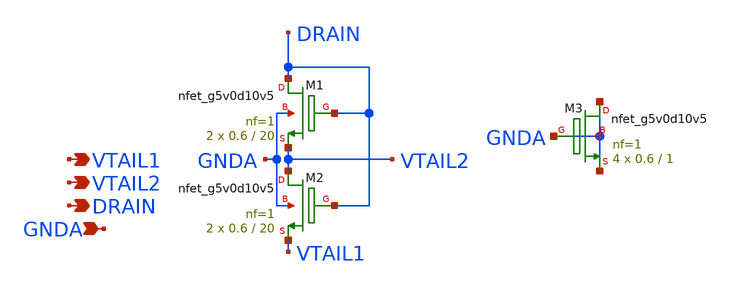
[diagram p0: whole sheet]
** sch_path: xschem/cm_ncell3.sch
**.subckt cm_ncell3 GNDA VTAIL1 VTAIL2 DRAIN
*.ipin GNDA
*.opin VTAIL1
*.opin VTAIL2
*.opin DRAIN
XM1 DRAIN DRAIN VTAIL2 GNDA sky130_fd_pr__nfet_g5v0d10v5 L=20 W=0.6 nf=1 ad='int((nf+1)/2) * W/nf * 0.29'
+ as='int((nf+2)/2) * W/nf * 0.29' pd='2*int((nf+1)/2) * (W/nf + 0.29)' ps='2*int((nf+2)/2) * (W/nf + 0.29)'
+ nrd='0.29 / W' nrs='0.29 / W' sa=0 sb=0 sd=0 mult=2 m=2
XM2 VTAIL2 DRAIN VTAIL1 GNDA sky130_fd_pr__nfet_g5v0d10v5 L=20 W=0.6 nf=1 ad='int((nf+1)/2) * W/nf * 0.29'
+ as='int((nf+2)/2) * W/nf * 0.29' pd='2*int((nf+1)/2) * (W/nf + 0.29)' ps='2*int((nf+2)/2) * (W/nf + 0.29)'
+ nrd='0.29 / W' nrs='0.29 / W' sa=0 sb=0 sd=0 mult=2 m=2
XM3 GNDA GNDA GNDA GNDA sky130_fd_pr__nfet_g5v0d10v5 L=1 W=0.6 nf=1 ad='int((nf+1)/2) * W/nf * 0.29'
+ as='int((nf+2)/2) * W/nf * 0.29' pd='2*int((nf+1)/2) * (W/nf + 0.29)' ps='2*int((nf+2)/2) * (W/nf + 0.29)'
+ nrd='0.29 / W' nrs='0.29 / W' sa=0 sb=0 sd=0 mult=4 m=4
**.ends
.end
